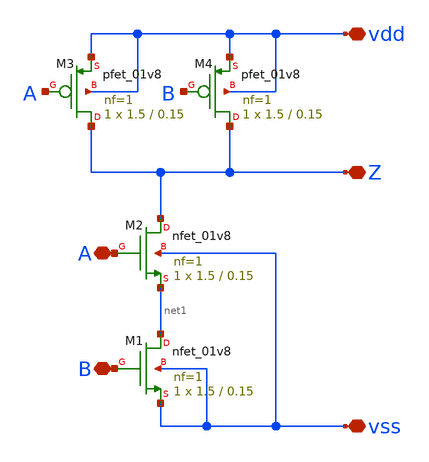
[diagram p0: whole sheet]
** sch_path: designs/nand.sch
**.subckt nand B A vdd Z vss
*.iopin B
*.iopin A
*.iopin vdd
*.iopin Z
*.iopin vss
XM1 net1 B vss vss sky130_fd_pr__nfet_01v8 L=0.15 W=1.5 nf=1 ad='int((nf+1)/2) * W/nf * 0.29' as='int((nf+2)/2) * W/nf * 0.29'
+ pd='2*int((nf+1)/2) * (W/nf + 0.29)' ps='2*int((nf+2)/2) * (W/nf + 0.29)' nrd='0.29 / W' nrs='0.29 / W'
+ sa=0 sb=0 sd=0 mult=1 m=1
XM2 Z A net1 vss sky130_fd_pr__nfet_01v8 L=0.15 W=1.5 nf=1 ad='int((nf+1)/2) * W/nf * 0.29' as='int((nf+2)/2) * W/nf * 0.29'
+ pd='2*int((nf+1)/2) * (W/nf + 0.29)' ps='2*int((nf+2)/2) * (W/nf + 0.29)' nrd='0.29 / W' nrs='0.29 / W'
+ sa=0 sb=0 sd=0 mult=1 m=1
XM3 Z A vdd vdd sky130_fd_pr__pfet_01v8 L=0.15 W=1.5 nf=1 ad='int((nf+1)/2) * W/nf * 0.29' as='int((nf+2)/2) * W/nf * 0.29'
+ pd='2*int((nf+1)/2) * (W/nf + 0.29)' ps='2*int((nf+2)/2) * (W/nf + 0.29)' nrd='0.29 / W' nrs='0.29 / W'
+ sa=0 sb=0 sd=0 mult=1 m=1
XM4 Z B vdd vdd sky130_fd_pr__pfet_01v8 L=0.15 W=1.5 nf=1 ad='int((nf+1)/2) * W/nf * 0.29' as='int((nf+2)/2) * W/nf * 0.29'
+ pd='2*int((nf+1)/2) * (W/nf + 0.29)' ps='2*int((nf+2)/2) * (W/nf + 0.29)' nrd='0.29 / W' nrs='0.29 / W'
+ sa=0 sb=0 sd=0 mult=1 m=1
**.ends
.end
